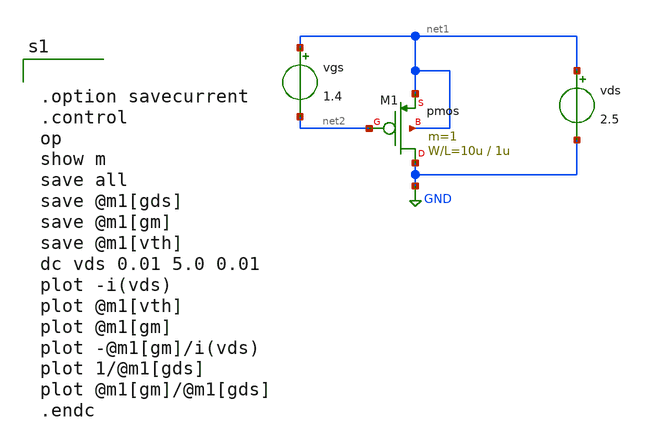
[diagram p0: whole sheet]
** sch_path: member_project/GroupWork/Team_masahiro/pfet_id-vds.sch
**.subckt pfet_id-vds
M1 GND net2 net1 net1 pmos L=1u W=10u m=1
vgs net1 net2 1.4
vds net1 GND 2.5
**** begin user architecture code
 .include $::LIB/mos.lib
.include $::LIB/passive.lib
.include $::LIB/diode.lib


.option savecurrent
.control
op
show m
save all
save @m1[gds]
save @m1[gm]
save @m1[vth]
dc vds 0.01 5.0 0.01
plot -i(vds)
plot @m1[vth]
plot @m1[gm]
plot -@m1[gm]/i(vds)
plot 1/@m1[gds]
plot @m1[gm]/@m1[gds]
.endc


**** end user architecture code
**.ends
.GLOBAL GND
.end
